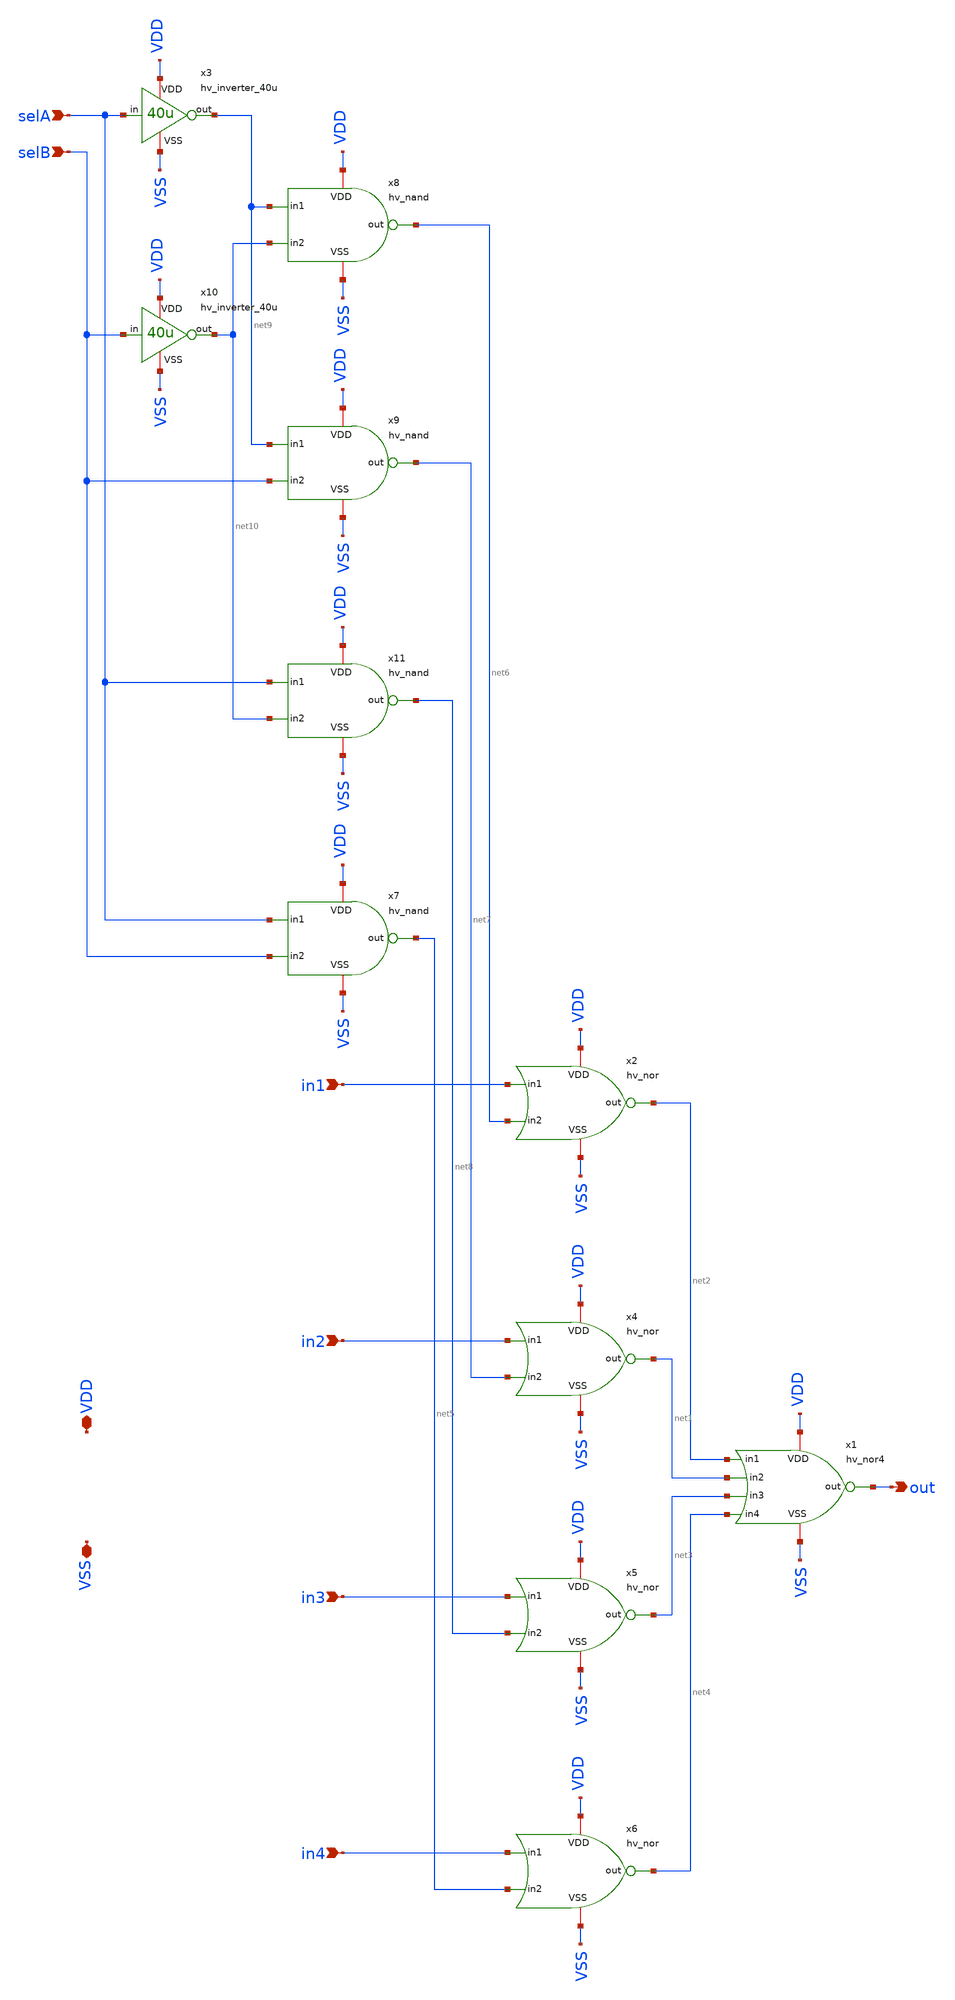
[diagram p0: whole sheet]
** sch_path: macros/heichips26_vcr/macros/switched_capacitor/schematic/xschem/hv_mux4.sch
**.subckt hv_mux4 in1 VDD VSS out in2 selA in3 in4 selB
*.ipin in1
*.iopin VDD
*.iopin VSS
*.opin out
*.ipin in2
*.ipin selA
*.ipin in3
*.ipin in4
*.ipin selB
x3 VDD selA net9 VSS hv_inverter_40u
x1 VDD net2 out net1 VSS net3 net4 hv_nor4
x2 VDD in1 net2 net6 VSS hv_nor
x4 VDD in2 net1 net7 VSS hv_nor
x5 VDD in3 net3 net8 VSS hv_nor
x6 VDD in4 net4 net5 VSS hv_nor
x7 VDD selA net5 selB VSS hv_nand
x9 VDD net9 net7 selB VSS hv_nand
x10 VDD selB net10 VSS hv_inverter_40u
x11 VDD selA net8 net10 VSS hv_nand
x8 VDD net9 net6 net10 VSS hv_nand
**.ends

* expanding   symbol:  hv_inverter_40u.sym # of pins=4
** sym_path: macros/heichips26_vcr/macros/switched_capacitor/schematic/xschem/hv_inverter_40u.sym
** sch_path: macros/heichips26_vcr/macros/switched_capacitor/schematic/xschem/hv_inverter_40u.sch
.subckt hv_inverter_40u VDD in out VSS
*.ipin in
*.iopin VDD
*.iopin VSS
*.opin out
XM2 out in VSS VSS sg13_hv_nmos w={n_w} l={n_l} ng={ng} m=1 mm_ok=1
XM3 out in VDD VDD sg13_hv_pmos w={p_w} l={p_l} ng={ng} m=1 mm_ok=1
**** begin user architecture code


.param w   = 10u
.param ng  = 4
.param n_ng = ng
.param n_w = {3u*n_ng}
.param n_l = 0.45u
.param p_ng = ng
.param p_w = {10u*p_ng}
.param p_l = 0.4u


**** end user architecture code
.ends


* expanding   symbol:  hv_nor4.sym # of pins=7
** sym_path: macros/heichips26_vcr/macros/switched_capacitor/schematic/xschem/hv_nor4.sym
** sch_path: macros/heichips26_vcr/macros/switched_capacitor/schematic/xschem/hv_nor4.sch
.subckt hv_nor4 VDD in1 out in2 VSS in3 in4
*.ipin in1
*.iopin VDD
*.iopin VSS
*.opin out
*.ipin in2
*.ipin in3
*.ipin in4
**** begin user architecture code


.param w   = 10u
.param ng  = 4
.param n_ng = ng
.param n_w = {3u*n_ng}
.param n_l = 0.45u
.param p_ng = ng
.param p_w = {10u*p_ng}
.param p_l = 0.4u


**** end user architecture code
XM2 out in3 VSS VSS sg13_hv_nmos w={n_w} l={n_l} ng={ng} m=1 mm_ok=1
XM3 net3 in4 VDD VDD sg13_hv_pmos w={p_w} l={p_l} ng={ng} m=1 mm_ok=1
XM1 out in4 VSS VSS sg13_hv_nmos w={n_w} l={n_l} ng={ng} m=1 mm_ok=1
XM4 out in1 net1 VDD sg13_hv_pmos w={p_w} l={p_l} ng={ng} m=1 mm_ok=1
XM5 out in2 VSS VSS sg13_hv_nmos w={n_w} l={n_l} ng={ng} m=1 mm_ok=1
XM6 out in1 VSS VSS sg13_hv_nmos w={n_w} l={n_l} ng={ng} m=1 mm_ok=1
XM7 net1 in2 net2 VDD sg13_hv_pmos w={p_w} l={p_l} ng={ng} m=1 mm_ok=1
XM8 net2 in3 net3 VDD sg13_hv_pmos w={p_w} l={p_l} ng={ng} m=1 mm_ok=1
.ends


* expanding   symbol:  hv_nor.sym # of pins=5
** sym_path: macros/heichips26_vcr/macros/switched_capacitor/schematic/xschem/hv_nor.sym
** sch_path: macros/heichips26_vcr/macros/switched_capacitor/schematic/xschem/hv_nor.sch
.subckt hv_nor VDD in1 out in2 VSS
*.ipin in1
*.iopin VDD
*.iopin VSS
*.opin out
*.ipin in2
**** begin user architecture code


.param w   = 10u
.param ng  = 4
.param n_ng = ng
.param n_w = {3u*n_ng}
.param n_l = 0.45u
.param p_ng = ng
.param p_w = {10u*p_ng}
.param p_l = 0.4u


**** end user architecture code
XM2 out in1 VSS VSS sg13_hv_nmos w={n_w} l={n_l} ng={ng} m=1 mm_ok=1
XM3 net1 in2 VDD VDD sg13_hv_pmos w={p_w} l={p_l} ng={ng} m=1 mm_ok=1
XM1 out in2 VSS VSS sg13_hv_nmos w={n_w} l={n_l} ng={ng} m=1 mm_ok=1
XM4 out in1 net1 VDD sg13_hv_pmos w={p_w} l={p_l} ng={ng} m=1 mm_ok=1
.ends


* expanding   symbol:  hv_nand.sym # of pins=5
** sym_path: macros/heichips26_vcr/macros/switched_capacitor/schematic/xschem/hv_nand.sym
** sch_path: macros/heichips26_vcr/macros/switched_capacitor/schematic/xschem/hv_nand.sch
.subckt hv_nand VDD in1 out in2 VSS
*.ipin in1
*.iopin VDD
*.iopin VSS
*.opin out
*.ipin in2
**** begin user architecture code


.param w   = 10u
.param ng  = 4
.param n_ng = ng
.param n_w = {3u*n_ng}
.param n_l = 0.45u
.param p_ng = ng
.param p_w = {10u*p_ng}
.param p_l = 0.4u


**** end user architecture code
XM2 out in1 net1 VSS sg13_hv_nmos w={n_w} l={n_l} ng={ng} m=1 mm_ok=1
XM3 out in2 VDD VDD sg13_hv_pmos w={p_w} l={p_l} ng={ng} m=1 mm_ok=1
XM1 net1 in2 VSS VSS sg13_hv_nmos w={n_w} l={n_l} ng={ng} m=1 mm_ok=1
XM4 out in1 VDD VDD sg13_hv_pmos w={p_w} l={p_l} ng={ng} m=1 mm_ok=1
.ends

.end
